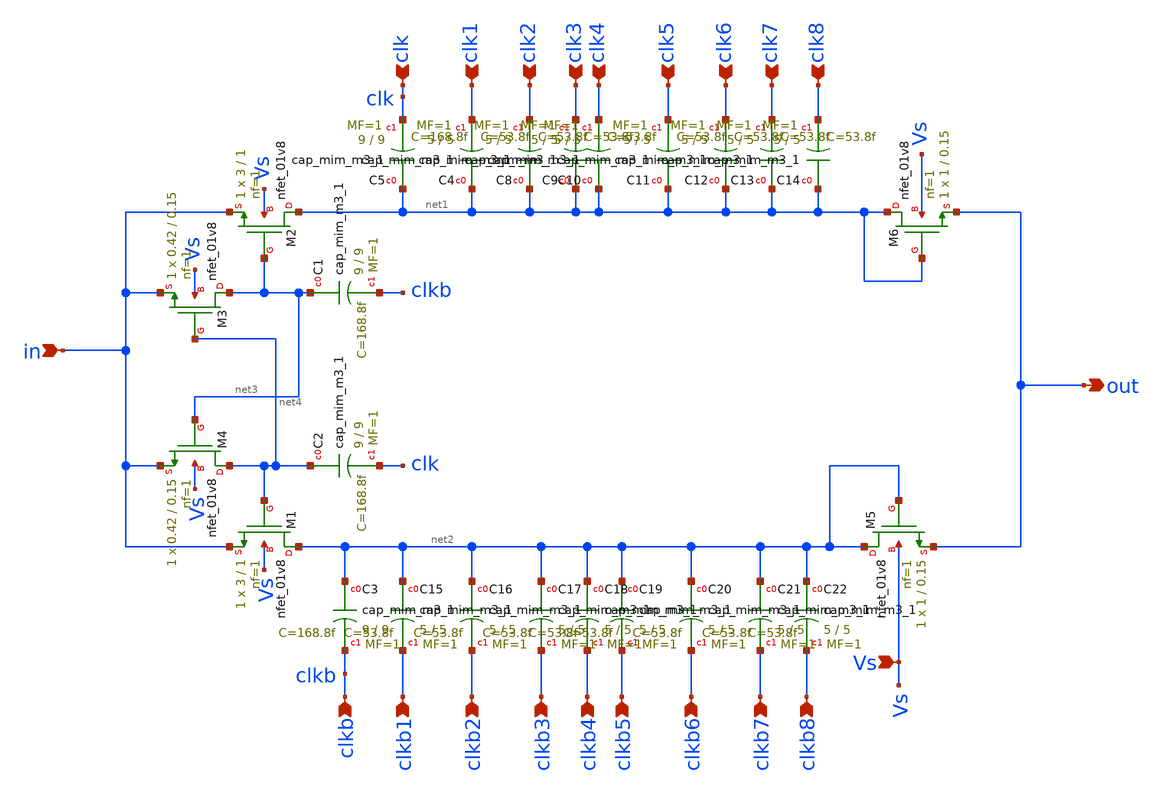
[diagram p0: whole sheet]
** sch_path: xschem/CP2_lvt.sch
**.subckt CP2_lvt in clk clk1 clk2 clk3 clk4 clk5 clk6 clk7 clk8 clkb clkb1 clkb2 clkb3 clkb4 clkb5
*+ clkb6 clkb7 clkb8 out Vs
*.ipin in
*.ipin clk
*.ipin clk1
*.ipin clk2
*.ipin clk3
*.ipin clk4
*.ipin clk5
*.ipin clk6
*.ipin clk7
*.ipin clk8
*.ipin clkb
*.ipin clkb1
*.ipin clkb2
*.ipin clkb3
*.ipin clkb4
*.ipin clkb5
*.ipin clkb6
*.ipin clkb7
*.ipin clkb8
*.opin out
*.ipin Vs
XM2 net1 net3 in Vs sky130_fd_pr__nfet_01v8 L=1 W=3 nf=1 ad='int((nf+1)/2) * W/nf * 0.29' as='int((nf+2)/2) * W/nf * 0.29'
+ pd='2*int((nf+1)/2) * (W/nf + 0.29)' ps='2*int((nf+2)/2) * (W/nf + 0.29)' nrd='0.29 / W' nrs='0.29 / W'
+ sa=0 sb=0 sd=0 mult=1 m=1
XM1 net2 net4 in Vs sky130_fd_pr__nfet_01v8 L=1 W=3 nf=1 ad='int((nf+1)/2) * W/nf * 0.29' as='int((nf+2)/2) * W/nf * 0.29'
+ pd='2*int((nf+1)/2) * (W/nf + 0.29)' ps='2*int((nf+2)/2) * (W/nf + 0.29)' nrd='0.29 / W' nrs='0.29 / W'
+ sa=0 sb=0 sd=0 mult=1 m=1
XM3 net3 net4 in Vs sky130_fd_pr__nfet_01v8 L=0.15 W=0.42 nf=1 ad='int((nf+1)/2) * W/nf * 0.29' as='int((nf+2)/2) * W/nf * 0.29'
+ pd='2*int((nf+1)/2) * (W/nf + 0.29)' ps='2*int((nf+2)/2) * (W/nf + 0.29)' nrd='0.29 / W' nrs='0.29 / W'
+ sa=0 sb=0 sd=0 mult=1 m=1
XM4 net4 net3 in Vs sky130_fd_pr__nfet_01v8 L=0.15 W=0.42 nf=1 ad='int((nf+1)/2) * W/nf * 0.29' as='int((nf+2)/2) * W/nf * 0.29'
+ pd='2*int((nf+1)/2) * (W/nf + 0.29)' ps='2*int((nf+2)/2) * (W/nf + 0.29)' nrd='0.29 / W' nrs='0.29 / W'
+ sa=0 sb=0 sd=0 mult=1 m=1
XC1 net3 clkb sky130_fd_pr__cap_mim_m3_1 W=9 L=9 MF=1 m=1
XC2 net4 clk sky130_fd_pr__cap_mim_m3_1 W=9 L=9 MF=1 m=1
XC5 net1 clk sky130_fd_pr__cap_mim_m3_1 W=9 L=9 MF=1 m=1
XC3 net2 clkb sky130_fd_pr__cap_mim_m3_1 W=9 L=9 MF=1 m=1
XC8 net1 clk2 sky130_fd_pr__cap_mim_m3_1 W=5 L=5 MF=1 m=1
XC9 net1 clk3 sky130_fd_pr__cap_mim_m3_1 W=5 L=5 MF=1 m=1
XC10 net1 clk4 sky130_fd_pr__cap_mim_m3_1 W=5 L=5 MF=1 m=1
XC11 net1 clk5 sky130_fd_pr__cap_mim_m3_1 W=5 L=5 MF=1 m=1
XC12 net1 clk6 sky130_fd_pr__cap_mim_m3_1 W=5 L=5 MF=1 m=1
XC13 net1 clk7 sky130_fd_pr__cap_mim_m3_1 W=5 L=5 MF=1 m=1
XC14 net1 clk8 sky130_fd_pr__cap_mim_m3_1 W=5 L=5 MF=1 m=1
XC15 net2 clkb1 sky130_fd_pr__cap_mim_m3_1 W=5 L=5 MF=1 m=1
XC16 net2 clkb2 sky130_fd_pr__cap_mim_m3_1 W=5 L=5 MF=1 m=1
XC17 net2 clkb3 sky130_fd_pr__cap_mim_m3_1 W=5 L=5 MF=1 m=1
XC18 net2 clkb4 sky130_fd_pr__cap_mim_m3_1 W=5 L=5 MF=1 m=1
XC19 net2 clkb5 sky130_fd_pr__cap_mim_m3_1 W=5 L=5 MF=1 m=1
XC20 net2 clkb6 sky130_fd_pr__cap_mim_m3_1 W=5 L=5 MF=1 m=1
XC21 net2 clkb7 sky130_fd_pr__cap_mim_m3_1 W=5 L=5 MF=1 m=1
XC22 net2 clkb8 sky130_fd_pr__cap_mim_m3_1 W=5 L=5 MF=1 m=1
XC4 net1 clk1 sky130_fd_pr__cap_mim_m3_1 W=5 L=5 MF=1 m=1
XM5 net2 net2 out Vs sky130_fd_pr__nfet_01v8 L=0.15 W=1 nf=1 ad='int((nf+1)/2) * W/nf * 0.29' as='int((nf+2)/2) * W/nf * 0.29'
+ pd='2*int((nf+1)/2) * (W/nf + 0.29)' ps='2*int((nf+2)/2) * (W/nf + 0.29)' nrd='0.29 / W' nrs='0.29 / W'
+ sa=0 sb=0 sd=0 mult=1 m=1
XM6 net1 net1 out Vs sky130_fd_pr__nfet_01v8 L=0.15 W=1 nf=1 ad='int((nf+1)/2) * W/nf * 0.29' as='int((nf+2)/2) * W/nf * 0.29'
+ pd='2*int((nf+1)/2) * (W/nf + 0.29)' ps='2*int((nf+2)/2) * (W/nf + 0.29)' nrd='0.29 / W' nrs='0.29 / W'
+ sa=0 sb=0 sd=0 mult=1 m=1
**.ends
.end
